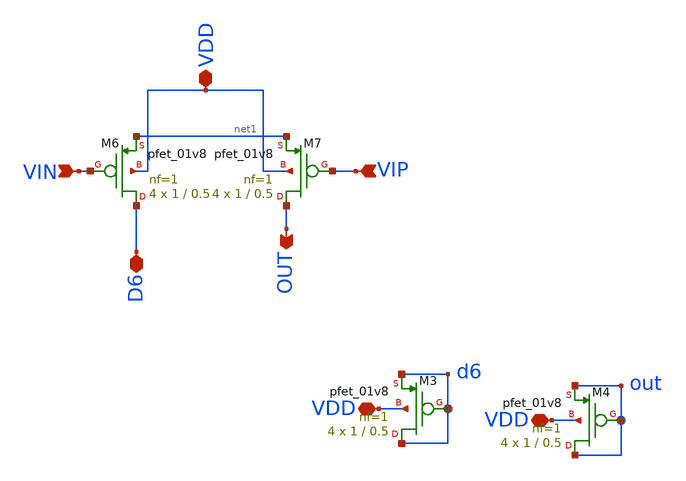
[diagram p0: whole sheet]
** sch_path: mag/lpmos.sch
**.subckt lpmos VIP VDD VIN OUT D6 VDD VDD
*.ipin VIP
*.iopin VDD
*.ipin VIN
*.opin OUT
*.iopin D6
*.iopin VDD
*.iopin VDD
XM7 OUT VIP net1 VDD sky130_fd_pr__pfet_01v8 L=0.5 W=1 nf=1 ad='int((nf+1)/2) * W/nf * 0.29' as='int((nf+2)/2) * W/nf * 0.29'
+ pd='2*int((nf+1)/2) * (W/nf + 0.29)' ps='2*int((nf+2)/2) * (W/nf + 0.29)' nrd='0.29 / W' nrs='0.29 / W'
+ sa=0 sb=0 sd=0 mult=4 m=4
XM6 D6 VIN net1 VDD sky130_fd_pr__pfet_01v8 L=0.5 W=1 nf=1 ad='int((nf+1)/2) * W/nf * 0.29' as='int((nf+2)/2) * W/nf * 0.29'
+ pd='2*int((nf+1)/2) * (W/nf + 0.29)' ps='2*int((nf+2)/2) * (W/nf + 0.29)' nrd='0.29 / W' nrs='0.29 / W'
+ sa=0 sb=0 sd=0 mult=4 m=4
XM3 d6 d6 d6 VDD sky130_fd_pr__pfet_01v8 L=0.5 W=1 nf=1 ad='int((nf+1)/2) * W/nf * 0.29' as='int((nf+2)/2) * W/nf * 0.29'
+ pd='2*int((nf+1)/2) * (W/nf + 0.29)' ps='2*int((nf+2)/2) * (W/nf + 0.29)' nrd='0.29 / W' nrs='0.29 / W'
+ sa=0 sb=0 sd=0 mult=4 m=4
XM4 out out out VDD sky130_fd_pr__pfet_01v8 L=0.5 W=1 nf=1 ad='int((nf+1)/2) * W/nf * 0.29' as='int((nf+2)/2) * W/nf * 0.29'
+ pd='2*int((nf+1)/2) * (W/nf + 0.29)' ps='2*int((nf+2)/2) * (W/nf + 0.29)' nrd='0.29 / W' nrs='0.29 / W'
+ sa=0 sb=0 sd=0 mult=4 m=4
**.ends
.end
